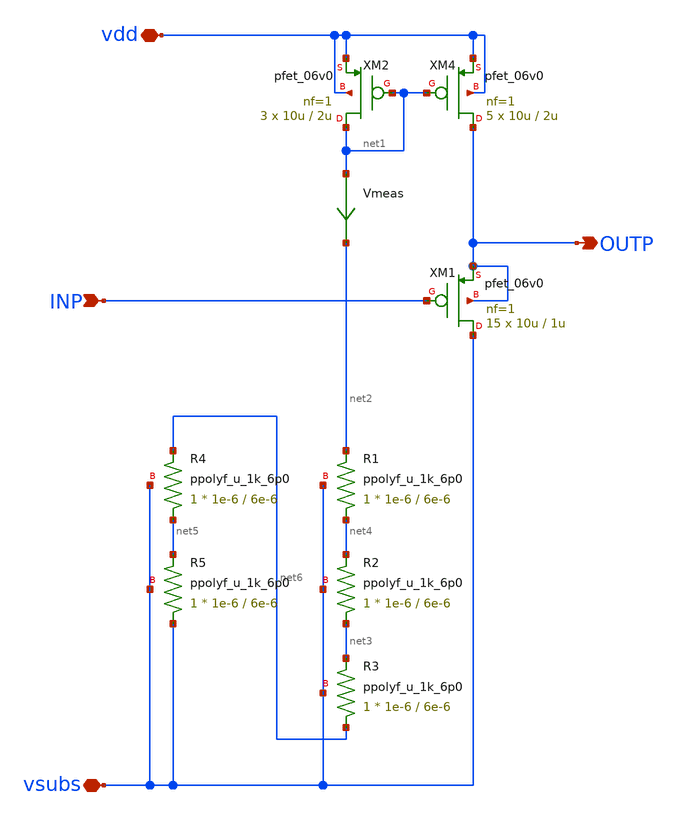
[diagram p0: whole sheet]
** sch_path: xschem/ip_buffer.sch
**.subckt ip_buffer vsubs vdd INP OUTP
*.iopin vsubs
*.iopin vdd
*.ipin INP
*.opin OUTP
XM1 vsubs INP OUTP OUTP pfet_06v0 L=1u W=10u nf=1 ad='int((nf+1)/2) * W/nf * 0.18u' as='int((nf+2)/2) * W/nf * 0.18u'
+ pd='2*int((nf+1)/2) * (W/nf + 0.18u)' ps='2*int((nf+2)/2) * (W/nf + 0.18u)' nrd='0.18u / W' nrs='0.18u / W'
+ sa=0 sb=0 sd=0 m=15
Vmeas net1 net2 0
XM4 OUTP net1 vdd vdd pfet_06v0 L=2u W=10u nf=1 ad='int((nf+1)/2) * W/nf * 0.18u' as='int((nf+2)/2) * W/nf * 0.18u'
+ pd='2*int((nf+1)/2) * (W/nf + 0.18u)' ps='2*int((nf+2)/2) * (W/nf + 0.18u)' nrd='0.18u / W' nrs='0.18u / W'
+ sa=0 sb=0 sd=0 m=5
XM2 net1 net1 vdd vdd pfet_06v0 L=2u W=10u nf=1 ad='int((nf+1)/2) * W/nf * 0.18u' as='int((nf+2)/2) * W/nf * 0.18u'
+ pd='2*int((nf+1)/2) * (W/nf + 0.18u)' ps='2*int((nf+2)/2) * (W/nf + 0.18u)' nrd='0.18u / W' nrs='0.18u / W'
+ sa=0 sb=0 sd=0 m=3
XR1 net4 net2 vsubs ppolyf_u_1k_6p0 r_width=1e-6 r_length=6e-6 m=1
XR2 net3 net4 vsubs ppolyf_u_1k_6p0 r_width=1e-6 r_length=6e-6 m=1
XR3 net6 net3 vsubs ppolyf_u_1k_6p0 r_width=1e-6 r_length=6e-6 m=1
XR4 net5 net6 vsubs ppolyf_u_1k_6p0 r_width=1e-6 r_length=6e-6 m=1
XR5 vsubs net5 vsubs ppolyf_u_1k_6p0 r_width=1e-6 r_length=6e-6 m=1
**.ends
.end
